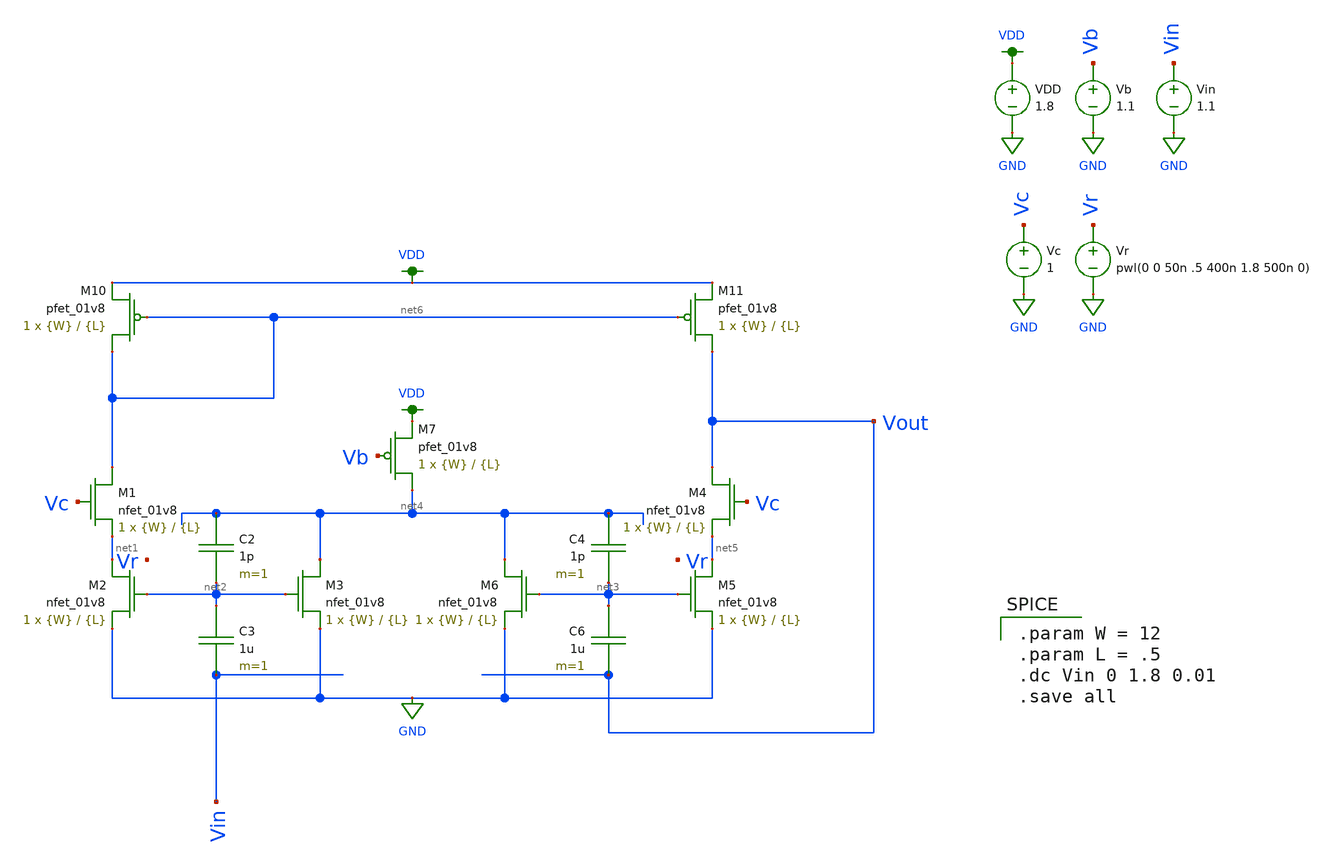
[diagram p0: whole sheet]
** sch_path: schematics/5_FGOP.sch
**.subckt 5_FGOP
XM1 net6 Vc net1 GND sky130_fd_pr__nfet_01v8 L={L} W={W} nf=1 ad='int((nf+1)/2) * W/nf * 0.29' as='int((nf+2)/2) * W/nf * 0.29'
+ pd='2*int((nf+1)/2) * (W/nf + 0.29)' ps='2*int((nf+2)/2) * (W/nf + 0.29)' nrd='0.29 / W' nrs='0.29 / W'
+ sa=0 sb=0 sd=0 mult=1 m=1
XM2 net1 net2 GND GND sky130_fd_pr__nfet_01v8 L={L} W={W} nf=1 ad='int((nf+1)/2) * W/nf * 0.29' as='int((nf+2)/2) * W/nf * 0.29'
+ pd='2*int((nf+1)/2) * (W/nf + 0.29)' ps='2*int((nf+2)/2) * (W/nf + 0.29)' nrd='0.29 / W' nrs='0.29 / W'
+ sa=0 sb=0 sd=0 mult=1 m=1
C2 net4 net2 1p m=1
C3 net2 Vin 1u m=1
XM3 net4 net2 GND GND sky130_fd_pr__nfet_01v8 L={L} W={W} nf=1 ad='int((nf+1)/2) * W/nf * 0.29' as='int((nf+2)/2) * W/nf * 0.29'
+ pd='2*int((nf+1)/2) * (W/nf + 0.29)' ps='2*int((nf+2)/2) * (W/nf + 0.29)' nrd='0.29 / W' nrs='0.29 / W'
+ sa=0 sb=0 sd=0 mult=1 m=1
XM4 Vout Vc net5 GND sky130_fd_pr__nfet_01v8 L={L} W={W} nf=1 ad='int((nf+1)/2) * W/nf * 0.29' as='int((nf+2)/2) * W/nf * 0.29'
+ pd='2*int((nf+1)/2) * (W/nf + 0.29)' ps='2*int((nf+2)/2) * (W/nf + 0.29)' nrd='0.29 / W' nrs='0.29 / W'
+ sa=0 sb=0 sd=0 mult=1 m=1
XM5 net5 net3 GND GND sky130_fd_pr__nfet_01v8 L={L} W={W} nf=1 ad='int((nf+1)/2) * W/nf * 0.29' as='int((nf+2)/2) * W/nf * 0.29'
+ pd='2*int((nf+1)/2) * (W/nf + 0.29)' ps='2*int((nf+2)/2) * (W/nf + 0.29)' nrd='0.29 / W' nrs='0.29 / W'
+ sa=0 sb=0 sd=0 mult=1 m=1
C4 net4 net3 1p m=1
C6 net3 Vout 1u m=1
XM6 net4 net3 GND GND sky130_fd_pr__nfet_01v8 L={L} W={W} nf=1 ad='int((nf+1)/2) * W/nf * 0.29' as='int((nf+2)/2) * W/nf * 0.29'
+ pd='2*int((nf+1)/2) * (W/nf + 0.29)' ps='2*int((nf+2)/2) * (W/nf + 0.29)' nrd='0.29 / W' nrs='0.29 / W'
+ sa=0 sb=0 sd=0 mult=1 m=1
XM7 net4 Vb VDD VDD sky130_fd_pr__pfet_01v8 L={L} W={W} nf=1 ad='int((nf+1)/2) * W/nf * 0.29' as='int((nf+2)/2) * W/nf * 0.29'
+ pd='2*int((nf+1)/2) * (W/nf + 0.29)' ps='2*int((nf+2)/2) * (W/nf + 0.29)' nrd='0.29 / W' nrs='0.29 / W'
+ sa=0 sb=0 sd=0 mult=1 m=1
VDD VDD GND 1.8
Vb Vb GND 1.1
Vc Vc GND 1
Vr Vr GND pwl(0 0 50n .5 400n 1.8 500n 0)
XM10 net6 net6 VDD VDD sky130_fd_pr__pfet_01v8 L={L} W={W} nf=1 ad='int((nf+1)/2) * W/nf * 0.29' as='int((nf+2)/2) * W/nf * 0.29'
+ pd='2*int((nf+1)/2) * (W/nf + 0.29)' ps='2*int((nf+2)/2) * (W/nf + 0.29)' nrd='0.29 / W' nrs='0.29 / W'
+ sa=0 sb=0 sd=0 mult=1 m=1
XM11 Vout net6 VDD VDD sky130_fd_pr__pfet_01v8 L={L} W={W} nf=1 ad='int((nf+1)/2) * W/nf * 0.29' as='int((nf+2)/2) * W/nf * 0.29'
+ pd='2*int((nf+1)/2) * (W/nf + 0.29)' ps='2*int((nf+2)/2) * (W/nf + 0.29)' nrd='0.29 / W' nrs='0.29 / W'
+ sa=0 sb=0 sd=0 mult=1 m=1
Vin Vin GND 1.1
**** begin user architecture code

.param W = 12
.param L = .5
.dc Vin 0 1.8 0.01
.save all


.option wnflag=1
.param MC_SWITCH=0.0
.lib ~/skywater/skywater-pdk/libraries/sky130_fd_pr_ngspice/latest/models/sky130.lib.spice tt

**** end user architecture code
**.ends
.GLOBAL GND
.GLOBAL VDD
.end
